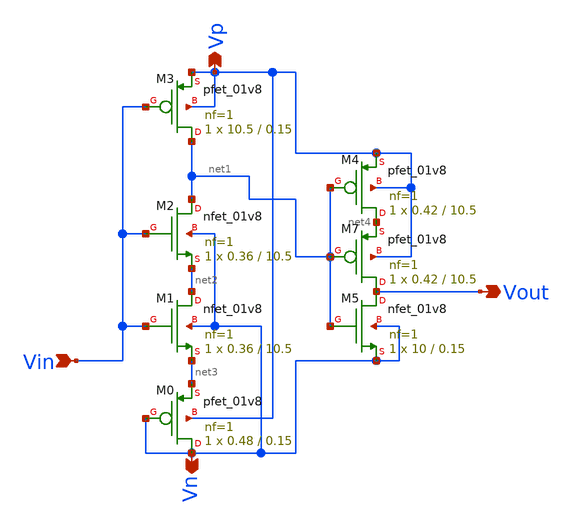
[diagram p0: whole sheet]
** sch_path: xschem/Vth_sch/Symbol/th15_backup.sch
**.subckt th15_backup Vin Vout Vp Vn
*.ipin Vin
*.opin Vout
*.opin Vp
*.opin Vn
XM0 Vn Vn net3 Vp sky130_fd_pr__pfet_01v8 L=0.15 W=0.48 nf=1 ad='int((nf+1)/2) * W/nf * 0.29' as='int((nf+2)/2) * W/nf * 0.29'
+ pd='2*int((nf+1)/2) * (W/nf + 0.29)' ps='2*int((nf+2)/2) * (W/nf + 0.29)' nrd='0.29 / W' nrs='0.29 / W'
+ sa=0 sb=0 sd=0 mult=1 m=1
XM1 net2 Vin net3 Vn sky130_fd_pr__nfet_01v8 L=10.5 W=0.36 nf=1 ad='int((nf+1)/2) * W/nf * 0.29' as='int((nf+2)/2) * W/nf * 0.29'
+ pd='2*int((nf+1)/2) * (W/nf + 0.29)' ps='2*int((nf+2)/2) * (W/nf + 0.29)' nrd='0.29 / W' nrs='0.29 / W'
+ sa=0 sb=0 sd=0 mult=1 m=1
XM2 net1 Vin net2 Vn sky130_fd_pr__nfet_01v8 L=10.5 W=0.36 nf=1 ad='int((nf+1)/2) * W/nf * 0.29' as='int((nf+2)/2) * W/nf * 0.29'
+ pd='2*int((nf+1)/2) * (W/nf + 0.29)' ps='2*int((nf+2)/2) * (W/nf + 0.29)' nrd='0.29 / W' nrs='0.29 / W'
+ sa=0 sb=0 sd=0 mult=1 m=1
XM3 net1 Vin Vp Vp sky130_fd_pr__pfet_01v8 L=0.15 W=10.5 nf=1 ad='int((nf+1)/2) * W/nf * 0.29' as='int((nf+2)/2) * W/nf * 0.29'
+ pd='2*int((nf+1)/2) * (W/nf + 0.29)' ps='2*int((nf+2)/2) * (W/nf + 0.29)' nrd='0.29 / W' nrs='0.29 / W'
+ sa=0 sb=0 sd=0 mult=1 m=1
XM4 net4 net1 Vp Vp sky130_fd_pr__pfet_01v8 L=10.5 W=0.42 nf=1 ad='int((nf+1)/2) * W/nf * 0.29' as='int((nf+2)/2) * W/nf * 0.29'
+ pd='2*int((nf+1)/2) * (W/nf + 0.29)' ps='2*int((nf+2)/2) * (W/nf + 0.29)' nrd='0.29 / W' nrs='0.29 / W'
+ sa=0 sb=0 sd=0 mult=1 m=1
XM7 Vout net1 net4 Vp sky130_fd_pr__pfet_01v8 L=10.5 W=0.42 nf=1 ad='int((nf+1)/2) * W/nf * 0.29' as='int((nf+2)/2) * W/nf * 0.29'
+ pd='2*int((nf+1)/2) * (W/nf + 0.29)' ps='2*int((nf+2)/2) * (W/nf + 0.29)' nrd='0.29 / W' nrs='0.29 / W'
+ sa=0 sb=0 sd=0 mult=1 m=1
XM5 Vout net1 Vn Vn sky130_fd_pr__nfet_01v8 L=0.15 W=10 nf=1 ad='int((nf+1)/2) * W/nf * 0.29' as='int((nf+2)/2) * W/nf * 0.29'
+ pd='2*int((nf+1)/2) * (W/nf + 0.29)' ps='2*int((nf+2)/2) * (W/nf + 0.29)' nrd='0.29 / W' nrs='0.29 / W'
+ sa=0 sb=0 sd=0 mult=1 m=1
**.ends
.end
